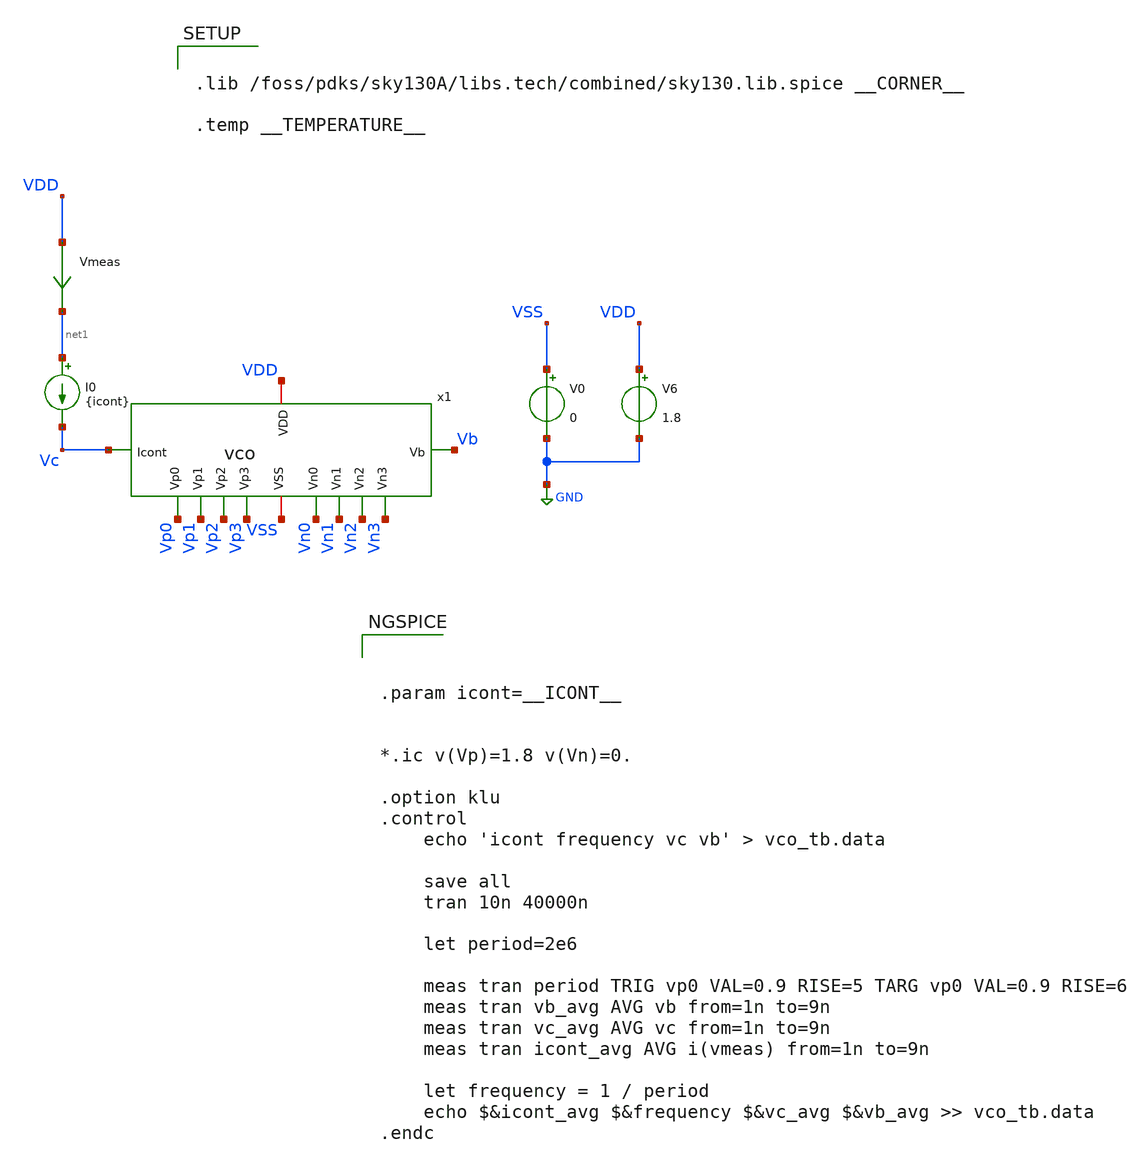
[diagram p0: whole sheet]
** sch_path: xschem-pex/vco_tb.sch
**.subckt vco_tb
V0 VSS GND 0
V6 VDD GND 1.8
I0 net1 Vc {icont}
x1 VDD VSS Vc Vp0 Vp1 Vp2 Vp3 Vn0 Vn1 Vn2 Vn3 Vb vco
Vmeas VDD net1 0
.save i(vmeas)
**** begin user architecture code



.param icont=__ICONT__


*.ic v(Vp)=1.8 v(Vn)=0.

.option klu
.control
	echo 'icont frequency vc vb' > vco_tb.data

	save all
	tran 10n 40000n

	let period=2e6

	meas tran period TRIG vp0 VAL=0.9 RISE=5 TARG vp0 VAL=0.9 RISE=6
	meas tran vb_avg AVG vb from=1n to=9n
	meas tran vc_avg AVG vc from=1n to=9n
	meas tran icont_avg AVG i(vmeas) from=1n to=9n

	let frequency = 1 / period
	echo $&icont_avg $&frequency $&vc_avg $&vb_avg >> vco_tb.data
.endc




.lib /foss/pdks/sky130A/libs.tech/combined/sky130.lib.spice __CORNER__

.temp __TEMPERATURE__


**** end user architecture code
**.ends

* expanding   symbol:  vco.sym # of pins=12
** sym_path: xschem-pex/vco.sym
.include ./vco.spice
.GLOBAL GND
.end
